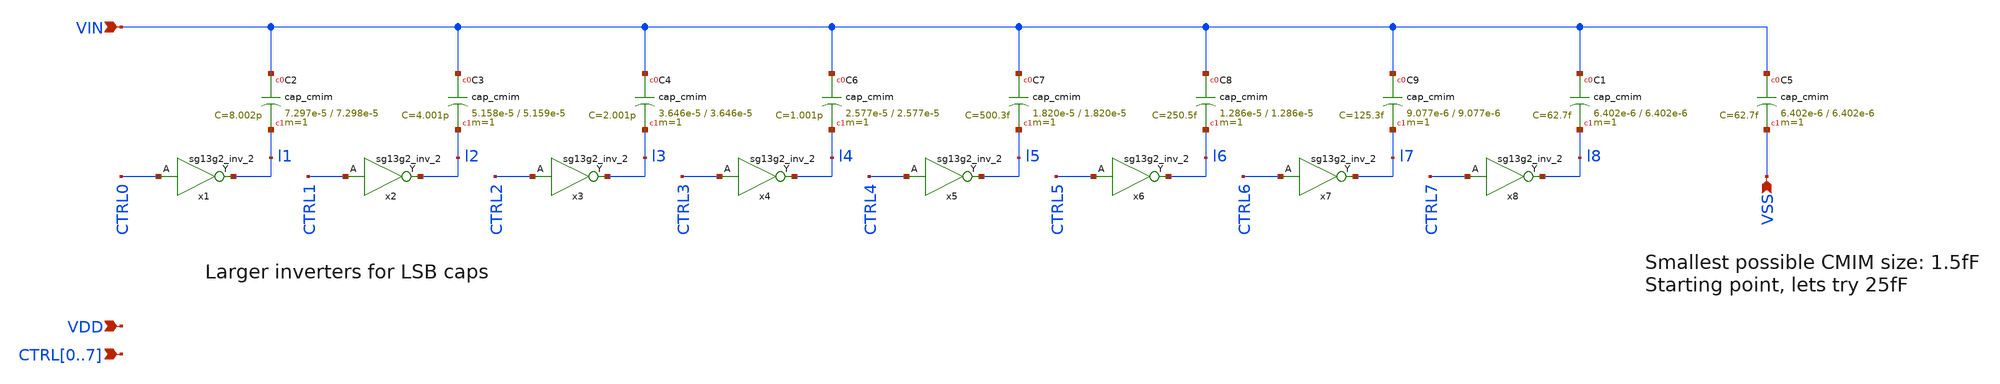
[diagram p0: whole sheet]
** sch_path: designs/cdac/cdac.sch
* IHP-GmbH/IHP-Open-PDK/ihp-sg13g2/libs.tech/xschem/sg13g2_stdcells/sg13g2_inv_2.sch:
* Copyright 2023 IHP PDK Authors
* Licensed under the Apache License, Version 2.0 (the "License");
**.subckt cdac VIN CTRL0,CTRL1,CTRL2,CTRL3,CTRL4,CTRL5,CTRL6,CTRL7 VSS VDD
*.ipin VIN
*.ipin CTRL0,CTRL1,CTRL2,CTRL3,CTRL4,CTRL5,CTRL6,CTRL7
*.ipin VSS
*.ipin VDD
XC2 VIN l1 cap_cmim w=7.297e-5 l=7.298e-5 m=1 mm_ok=1
XC3 VIN l2 cap_cmim w=5.158e-5 l=5.159e-5 m=1 mm_ok=1
XC4 VIN l3 cap_cmim w=3.646e-5 l=3.646e-5 m=1 mm_ok=1
XC5 VIN VSS cap_cmim w=6.402e-6 l=6.402e-6 m=1 mm_ok=1
x1 l1 CTRL0 VDD VSS sg13g2_inv_2
x2 l2 CTRL1 VDD VSS sg13g2_inv_2
x3 l3 CTRL2 VDD VSS sg13g2_inv_2
x4 l4 CTRL3 VDD VSS sg13g2_inv_2
XC6 VIN l4 cap_cmim w=2.577e-5 l=2.577e-5 m=1 mm_ok=1
XC7 VIN l5 cap_cmim w=1.820e-5 l=1.820e-5 m=1 mm_ok=1
XC8 VIN l6 cap_cmim w=1.286e-5 l=1.286e-5 m=1 mm_ok=1
XC9 VIN l7 cap_cmim w=9.077e-6 l=9.077e-6 m=1 mm_ok=1
x5 l5 CTRL4 VDD VSS sg13g2_inv_2
x6 l6 CTRL5 VDD VSS sg13g2_inv_2
x7 l7 CTRL6 VDD VSS sg13g2_inv_2
x8 l8 CTRL7 VDD VSS sg13g2_inv_2
XC1 VIN l8 cap_cmim w=6.402e-6 l=6.402e-6 m=1 mm_ok=1
**.ends

* expanding   symbol:  sg13g2_stdcells/sg13g2_inv_2.sym # of pins=2
** sym_path: sg13g2_stdcells/sg13g2_inv_2.sym
** sch_path: sg13g2_stdcells/sg13g2_inv_2.sch
.subckt sg13g2_inv_2 Y A VDD VSS
*.opin Y
*.ipin A
*.iopin VDD
*.iopin VSS
XM1 Y A VSS VSS sg13_lv_nmos w=1.48u l=130.00n ng=2 m=1 mm_ok=1
XM2 Y A VDD VDD sg13_lv_pmos w=2.24u l=130.00n ng=2 m=1 mm_ok=1
.ends

.end
